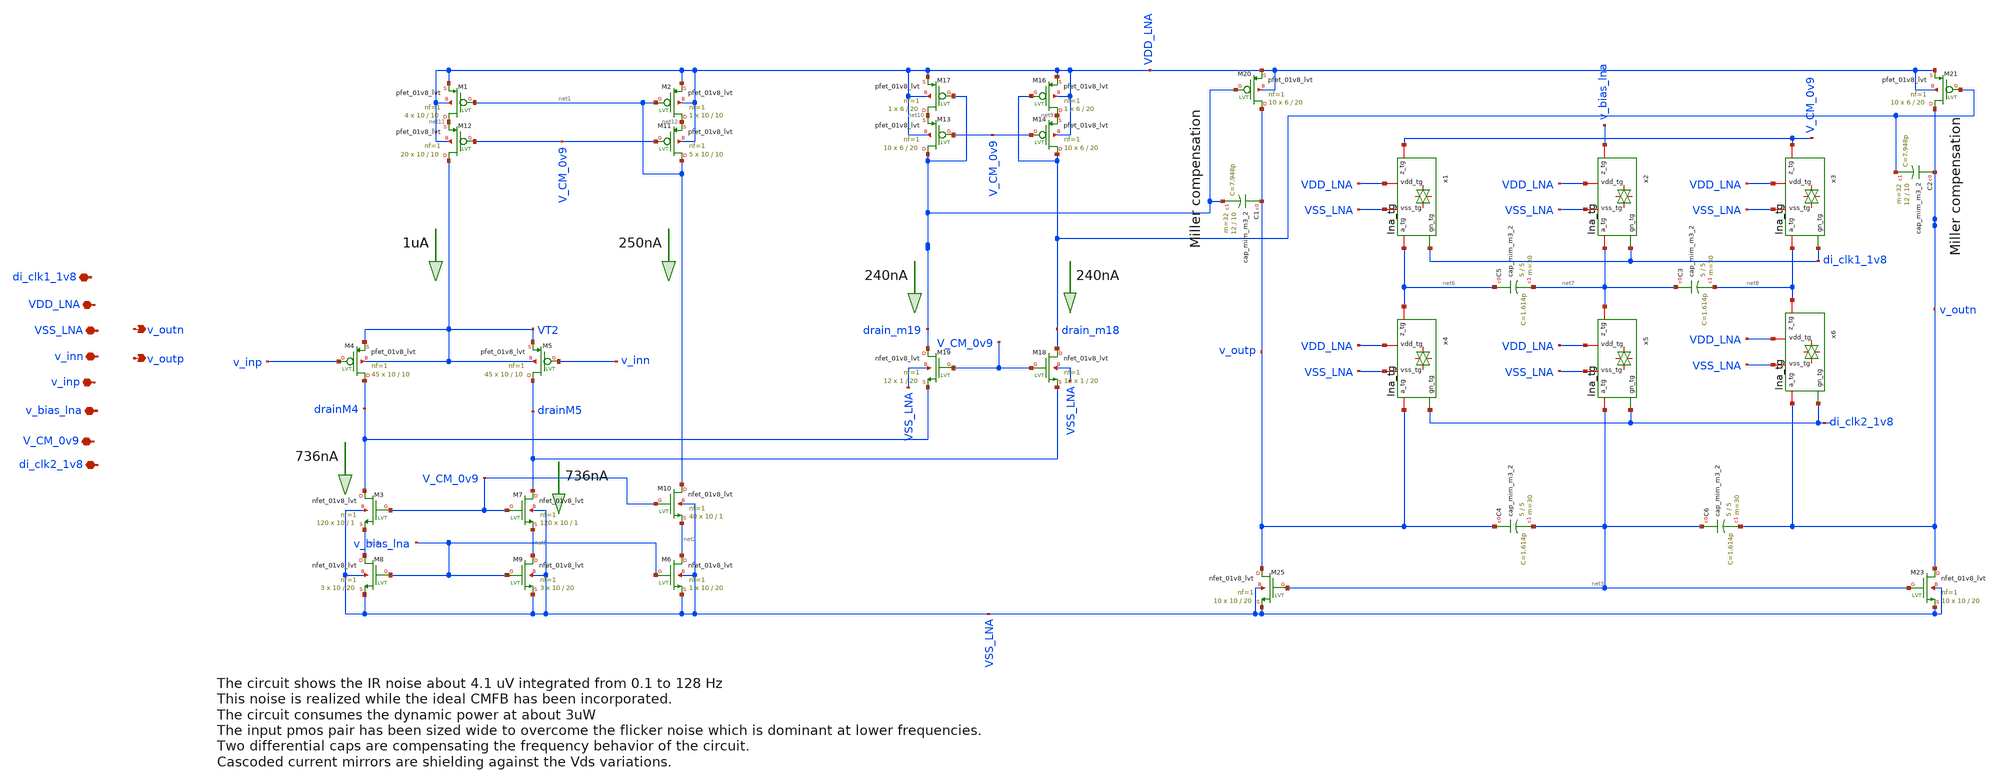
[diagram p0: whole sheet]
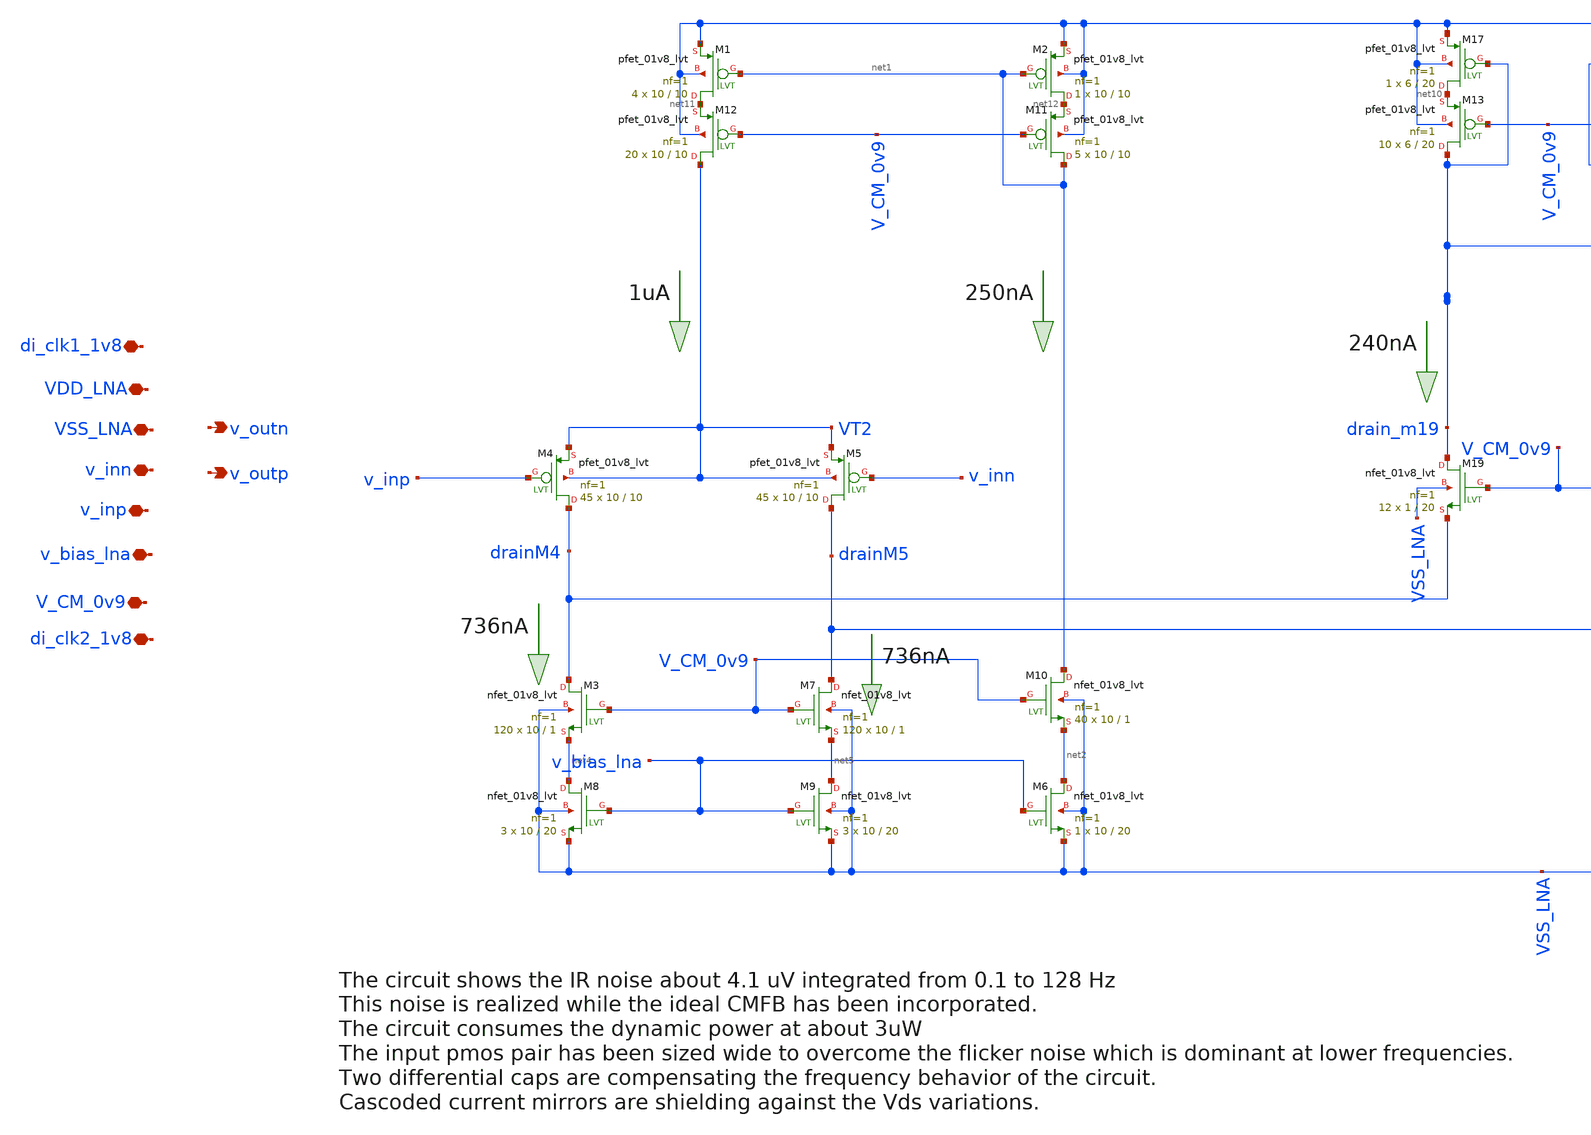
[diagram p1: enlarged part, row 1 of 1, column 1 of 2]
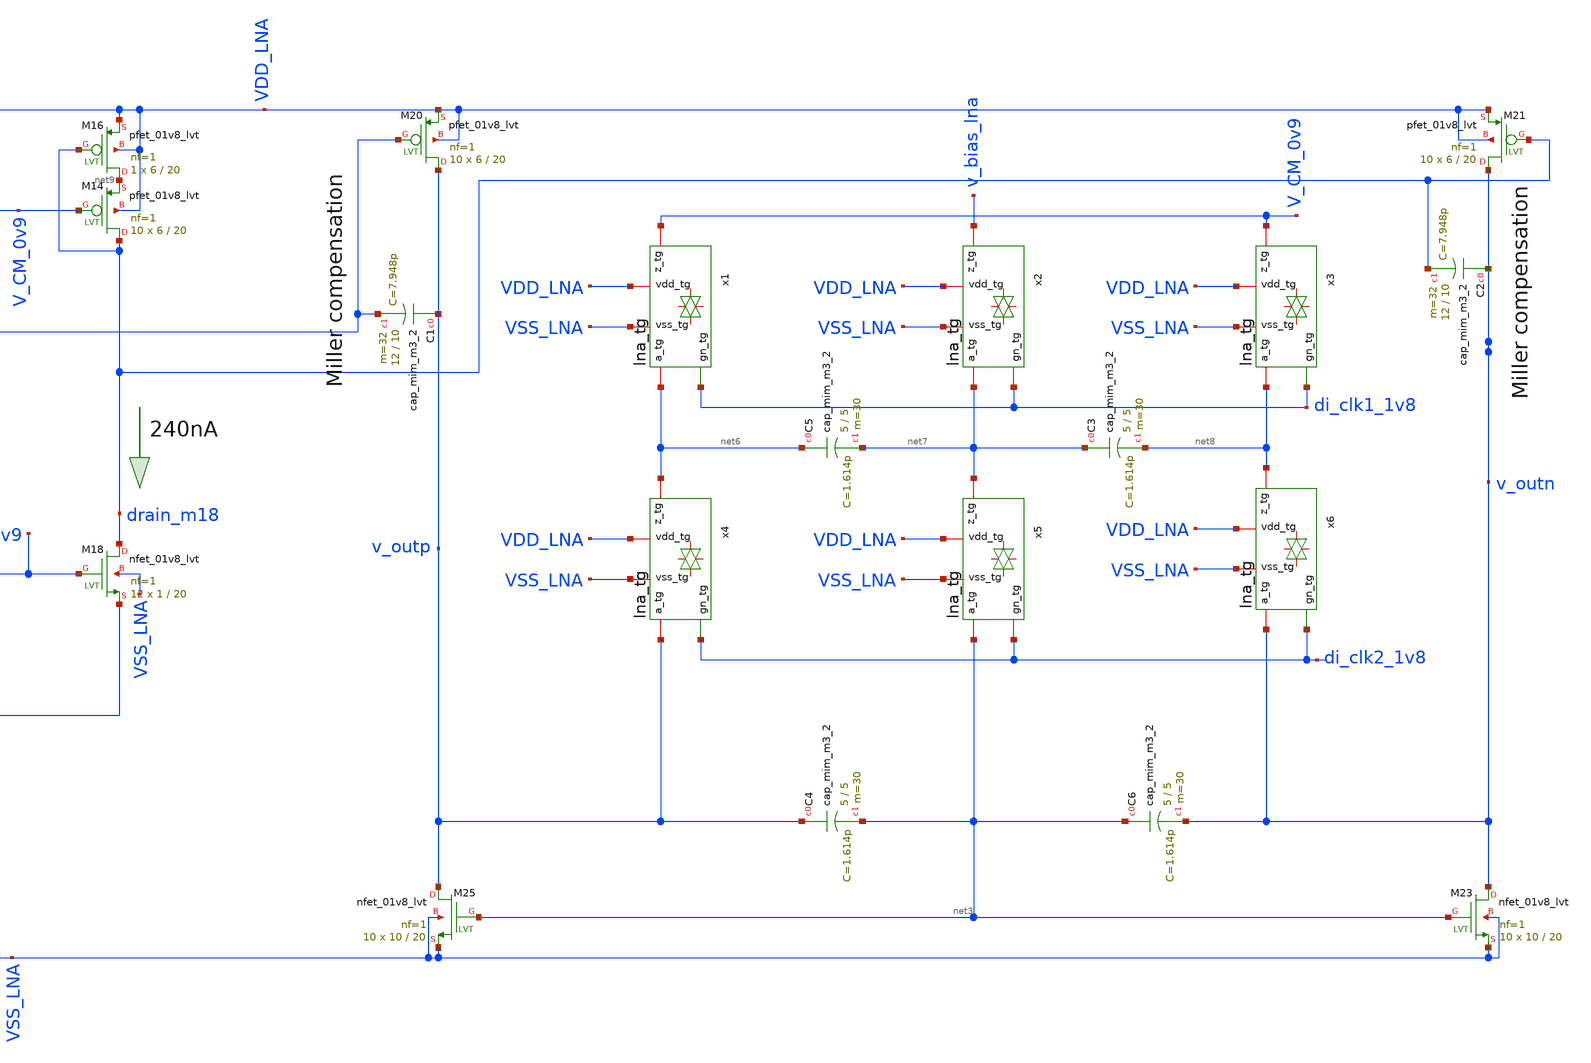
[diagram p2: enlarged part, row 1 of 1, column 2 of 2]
** sch_path: lna_core.sch
**.subckt lna_core v_inp v_inn VSS_LNA VDD_LNA V_CM_0v9 v_outp v_outn di_clk2_1v8 v_bias_lna
*+ di_clk1_1v8
*.iopin v_inp
*.iopin v_inn
*.iopin VSS_LNA
*.iopin VDD_LNA
*.iopin V_CM_0v9
*.opin v_outp
*.opin v_outn
*.iopin di_clk2_1v8
*.iopin v_bias_lna
*.iopin di_clk1_1v8
XM4 drainM4 v_inp VT2 VT2 sky130_fd_pr__pfet_01v8_lvt L=10 W=10 nf=1 ad='int((nf+1)/2) * W/nf * 0.29'
+ as='int((nf+2)/2) * W/nf * 0.29' pd='2*int((nf+1)/2) * (W/nf + 0.29)' ps='2*int((nf+2)/2) * (W/nf + 0.29)'
+ nrd='0.29 / W' nrs='0.29 / W' sa=0 sb=0 sd=0 mult=45 m=45
XM5 drainM5 v_inn VT2 VT2 sky130_fd_pr__pfet_01v8_lvt L=10 W=10 nf=1 ad='int((nf+1)/2) * W/nf * 0.29'
+ as='int((nf+2)/2) * W/nf * 0.29' pd='2*int((nf+1)/2) * (W/nf + 0.29)' ps='2*int((nf+2)/2) * (W/nf + 0.29)'
+ nrd='0.29 / W' nrs='0.29 / W' sa=0 sb=0 sd=0 mult=45 m=45
XM8 net4 v_bias_lna VSS_LNA VSS_LNA sky130_fd_pr__nfet_01v8_lvt L=20 W=10 nf=1 ad='int((nf+1)/2) * W/nf * 0.29'
+ as='int((nf+2)/2) * W/nf * 0.29' pd='2*int((nf+1)/2) * (W/nf + 0.29)' ps='2*int((nf+2)/2) * (W/nf + 0.29)'
+ nrd='0.29 / W' nrs='0.29 / W' sa=0 sb=0 sd=0 mult=3 m=3
XM9 net5 v_bias_lna VSS_LNA VSS_LNA sky130_fd_pr__nfet_01v8_lvt L=20 W=10 nf=1 ad='int((nf+1)/2) * W/nf * 0.29'
+ as='int((nf+2)/2) * W/nf * 0.29' pd='2*int((nf+1)/2) * (W/nf + 0.29)' ps='2*int((nf+2)/2) * (W/nf + 0.29)'
+ nrd='0.29 / W' nrs='0.29 / W' sa=0 sb=0 sd=0 mult=3 m=3
XM16 net9 drain_m18 VDD_LNA VDD_LNA sky130_fd_pr__pfet_01v8_lvt L=20 W=6 nf=1 ad='int((nf+1)/2) * W/nf * 0.29'
+ as='int((nf+2)/2) * W/nf * 0.29' pd='2*int((nf+1)/2) * (W/nf + 0.29)' ps='2*int((nf+2)/2) * (W/nf + 0.29)'
+ nrd='0.29 / W' nrs='0.29 / W' sa=0 sb=0 sd=0 mult=1 m=1
XM17 net10 drain_m19 VDD_LNA VDD_LNA sky130_fd_pr__pfet_01v8_lvt L=20 W=6 nf=1 ad='int((nf+1)/2) * W/nf * 0.29'
+ as='int((nf+2)/2) * W/nf * 0.29' pd='2*int((nf+1)/2) * (W/nf + 0.29)' ps='2*int((nf+2)/2) * (W/nf + 0.29)'
+ nrd='0.29 / W' nrs='0.29 / W' sa=0 sb=0 sd=0 mult=1 m=1
XM18 drain_m18 V_CM_0v9 drainM5 VSS_LNA sky130_fd_pr__nfet_01v8_lvt L=20 W=1 nf=1 ad='int((nf+1)/2) * W/nf * 0.29'
+ as='int((nf+2)/2) * W/nf * 0.29' pd='2*int((nf+1)/2) * (W/nf + 0.29)' ps='2*int((nf+2)/2) * (W/nf + 0.29)'
+ nrd='0.29 / W' nrs='0.29 / W' sa=0 sb=0 sd=0 mult=12 m=12
XM19 drain_m19 V_CM_0v9 drainM4 VSS_LNA sky130_fd_pr__nfet_01v8_lvt L=20 W=1 nf=1 ad='int((nf+1)/2) * W/nf * 0.29'
+ as='int((nf+2)/2) * W/nf * 0.29' pd='2*int((nf+1)/2) * (W/nf + 0.29)' ps='2*int((nf+2)/2) * (W/nf + 0.29)'
+ nrd='0.29 / W' nrs='0.29 / W' sa=0 sb=0 sd=0 mult=12 m=12
XM20 v_outp drain_m19 VDD_LNA VDD_LNA sky130_fd_pr__pfet_01v8_lvt L=20 W=6 nf=1 ad='int((nf+1)/2) * W/nf * 0.29'
+ as='int((nf+2)/2) * W/nf * 0.29' pd='2*int((nf+1)/2) * (W/nf + 0.29)' ps='2*int((nf+2)/2) * (W/nf + 0.29)'
+ nrd='0.29 / W' nrs='0.29 / W' sa=0 sb=0 sd=0 mult=10 m=10
XM21 v_outn drain_m18 VDD_LNA VDD_LNA sky130_fd_pr__pfet_01v8_lvt L=20 W=6 nf=1 ad='int((nf+1)/2) * W/nf * 0.29'
+ as='int((nf+2)/2) * W/nf * 0.29' pd='2*int((nf+1)/2) * (W/nf + 0.29)' ps='2*int((nf+2)/2) * (W/nf + 0.29)'
+ nrd='0.29 / W' nrs='0.29 / W' sa=0 sb=0 sd=0 mult=10 m=10
XM23 v_outn net3 VSS_LNA VSS_LNA sky130_fd_pr__nfet_01v8_lvt L=20 W=10 nf=1 ad='int((nf+1)/2) * W/nf * 0.29'
+ as='int((nf+2)/2) * W/nf * 0.29' pd='2*int((nf+1)/2) * (W/nf + 0.29)' ps='2*int((nf+2)/2) * (W/nf + 0.29)'
+ nrd='0.29 / W' nrs='0.29 / W' sa=0 sb=0 sd=0 mult=10 m=10
XM25 v_outp net3 VSS_LNA VSS_LNA sky130_fd_pr__nfet_01v8_lvt L=20 W=10 nf=1 ad='int((nf+1)/2) * W/nf * 0.29'
+ as='int((nf+2)/2) * W/nf * 0.29' pd='2*int((nf+1)/2) * (W/nf + 0.29)' ps='2*int((nf+2)/2) * (W/nf + 0.29)'
+ nrd='0.29 / W' nrs='0.29 / W' sa=0 sb=0 sd=0 mult=10 m=10
XM1 net11 net1 VDD_LNA VDD_LNA sky130_fd_pr__pfet_01v8_lvt L=10 W=10 nf=1 ad='int((nf+1)/2) * W/nf * 0.29'
+ as='int((nf+2)/2) * W/nf * 0.29' pd='2*int((nf+1)/2) * (W/nf + 0.29)' ps='2*int((nf+2)/2) * (W/nf + 0.29)'
+ nrd='0.29 / W' nrs='0.29 / W' sa=0 sb=0 sd=0 mult=4 m=4
XM2 net12 net1 VDD_LNA VDD_LNA sky130_fd_pr__pfet_01v8_lvt L=10 W=10 nf=1 ad='int((nf+1)/2) * W/nf * 0.29'
+ as='int((nf+2)/2) * W/nf * 0.29' pd='2*int((nf+1)/2) * (W/nf + 0.29)' ps='2*int((nf+2)/2) * (W/nf + 0.29)'
+ nrd='0.29 / W' nrs='0.29 / W' sa=0 sb=0 sd=0 mult=1 m=1
XM6 net2 v_bias_lna VSS_LNA VSS_LNA sky130_fd_pr__nfet_01v8_lvt L=20 W=10 nf=1 ad='int((nf+1)/2) * W/nf * 0.29'
+ as='int((nf+2)/2) * W/nf * 0.29' pd='2*int((nf+1)/2) * (W/nf + 0.29)' ps='2*int((nf+2)/2) * (W/nf + 0.29)'
+ nrd='0.29 / W' nrs='0.29 / W' sa=0 sb=0 sd=0 mult=1 m=1
XC1 v_outp drain_m19 sky130_fd_pr__cap_mim_m3_2 W=12 L=10 MF=32 m=32
XC2 v_outn drain_m18 sky130_fd_pr__cap_mim_m3_2 W=12 L=10 MF=32 m=32
x1 VDD_LNA net6 V_CM_0v9 VSS_LNA di_clk1_1v8 lna_tg
x2 VDD_LNA net7 v_bias_lna VSS_LNA di_clk1_1v8 lna_tg
x3 VDD_LNA net8 V_CM_0v9 VSS_LNA di_clk1_1v8 lna_tg
x4 VDD_LNA v_outp net6 VSS_LNA di_clk2_1v8 lna_tg
x5 VDD_LNA net3 net7 VSS_LNA di_clk2_1v8 lna_tg
XC5 net6 net7 sky130_fd_pr__cap_mim_m3_2 W=5 L=5 MF=30 m=30
x6 VDD_LNA v_outn net8 VSS_LNA di_clk2_1v8 lna_tg
XC3 net7 net8 sky130_fd_pr__cap_mim_m3_2 W=5 L=5 MF=30 m=30
XC4 v_outp net3 sky130_fd_pr__cap_mim_m3_2 W=5 L=5 MF=30 m=30
XC6 net3 v_outn sky130_fd_pr__cap_mim_m3_2 W=5 L=5 MF=30 m=30
XM3 drainM4 V_CM_0v9 net4 VSS_LNA sky130_fd_pr__nfet_01v8_lvt L=1 W=10 nf=1 ad='int((nf+1)/2) * W/nf * 0.29'
+ as='int((nf+2)/2) * W/nf * 0.29' pd='2*int((nf+1)/2) * (W/nf + 0.29)' ps='2*int((nf+2)/2) * (W/nf + 0.29)'
+ nrd='0.29 / W' nrs='0.29 / W' sa=0 sb=0 sd=0 mult=120 m=120
XM7 drainM5 V_CM_0v9 net5 VSS_LNA sky130_fd_pr__nfet_01v8_lvt L=1 W=10 nf=1 ad='int((nf+1)/2) * W/nf * 0.29'
+ as='int((nf+2)/2) * W/nf * 0.29' pd='2*int((nf+1)/2) * (W/nf + 0.29)' ps='2*int((nf+2)/2) * (W/nf + 0.29)'
+ nrd='0.29 / W' nrs='0.29 / W' sa=0 sb=0 sd=0 mult=120 m=120
XM10 net1 V_CM_0v9 net2 VSS_LNA sky130_fd_pr__nfet_01v8_lvt L=1 W=10 nf=1 ad='int((nf+1)/2) * W/nf * 0.29'
+ as='int((nf+2)/2) * W/nf * 0.29' pd='2*int((nf+1)/2) * (W/nf + 0.29)' ps='2*int((nf+2)/2) * (W/nf + 0.29)'
+ nrd='0.29 / W' nrs='0.29 / W' sa=0 sb=0 sd=0 mult=40 m=40
XM11 net1 V_CM_0v9 net12 VDD_LNA sky130_fd_pr__pfet_01v8_lvt L=10 W=10 nf=1 ad='int((nf+1)/2) * W/nf * 0.29'
+ as='int((nf+2)/2) * W/nf * 0.29' pd='2*int((nf+1)/2) * (W/nf + 0.29)' ps='2*int((nf+2)/2) * (W/nf + 0.29)'
+ nrd='0.29 / W' nrs='0.29 / W' sa=0 sb=0 sd=0 mult=5 m=5
XM12 VT2 V_CM_0v9 net11 VDD_LNA sky130_fd_pr__pfet_01v8_lvt L=10 W=10 nf=1 ad='int((nf+1)/2) * W/nf * 0.29'
+ as='int((nf+2)/2) * W/nf * 0.29' pd='2*int((nf+1)/2) * (W/nf + 0.29)' ps='2*int((nf+2)/2) * (W/nf + 0.29)'
+ nrd='0.29 / W' nrs='0.29 / W' sa=0 sb=0 sd=0 mult=20 m=20
XM13 drain_m19 V_CM_0v9 net10 VDD_LNA sky130_fd_pr__pfet_01v8_lvt L=20 W=6 nf=1 ad='int((nf+1)/2) * W/nf * 0.29'
+ as='int((nf+2)/2) * W/nf * 0.29' pd='2*int((nf+1)/2) * (W/nf + 0.29)' ps='2*int((nf+2)/2) * (W/nf + 0.29)'
+ nrd='0.29 / W' nrs='0.29 / W' sa=0 sb=0 sd=0 mult=10 m=10
XM14 drain_m18 V_CM_0v9 net9 VDD_LNA sky130_fd_pr__pfet_01v8_lvt L=20 W=6 nf=1 ad='int((nf+1)/2) * W/nf * 0.29'
+ as='int((nf+2)/2) * W/nf * 0.29' pd='2*int((nf+1)/2) * (W/nf + 0.29)' ps='2*int((nf+2)/2) * (W/nf + 0.29)'
+ nrd='0.29 / W' nrs='0.29 / W' sa=0 sb=0 sd=0 mult=10 m=10
**.ends
.end
